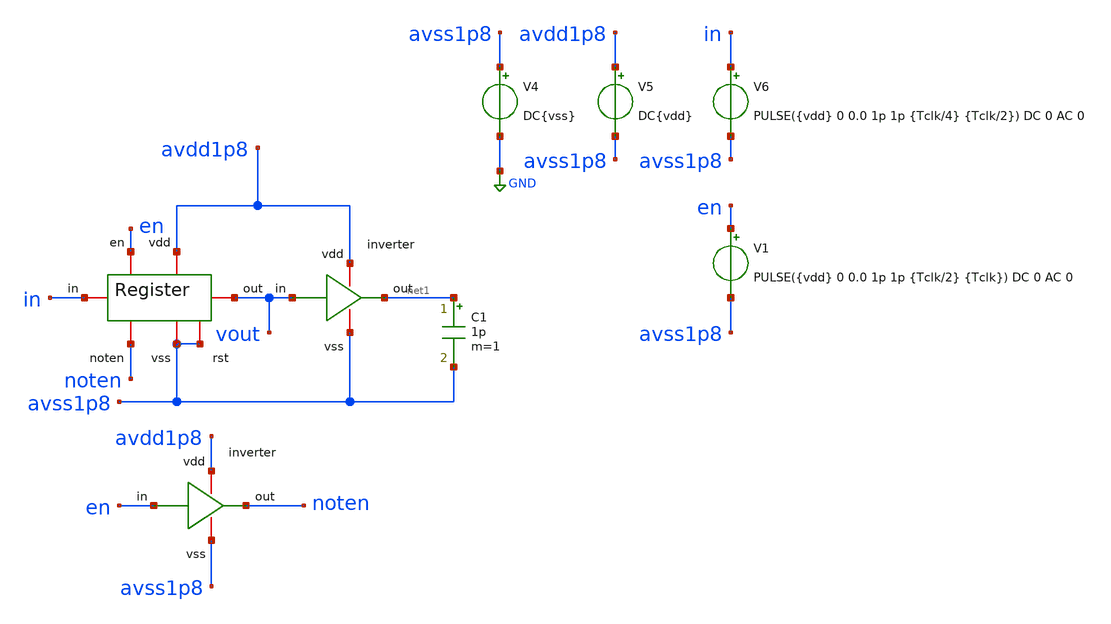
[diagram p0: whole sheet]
** sch_path: verification/testbenches/tb_register.sch
**.subckt tb_register
C1 net1 avss1p8 1p m=1
V4 avss1p8 GND DC{vss}
V5 avdd1p8 avss1p8 DC{vdd}
V6 in avss1p8 PULSE({vdd} 0 0.0 1p 1p {Tclk/4} {Tclk/2}) DC 0 AC 0
x2 avdd1p8 net1 vout avss1p8 inverter
V1 en avss1p8 PULSE({vdd} 0 0.0 1p 1p {Tclk/2} {Tclk}) DC 0 AC 0
x3 avdd1p8 noten en avss1p8 inverter
x1 en noten avss1p8 avdd1p8 vout in avss1p8 register
**** begin user architecture code


* Circuit Parameters
.param vdd = 1.2
.param vss = 0.0
.param Tclk = 10n
.options TEMP = 27.0
* Include Models - IHP SG13G2
.lib cornerMOSlv.lib mos_tt
* OP Parameters & Singals to save
.save all
*Simulations
.control
tran 0.01u 100n
setplot tran1
plot v(en) v(in) + 1.2 v(vout) + 2.4
set filetype = ascii
write dcsweep.raw
.endc
.end


**** end user architecture code
**.ends

* expanding   symbol:  blocks/inverter/schematic/inverter.sym # of pins=4
** sym_path: design/blocks/inverter/schematic/inverter.sym
** sch_path: design/blocks/inverter/schematic/inverter.sch
.subckt inverter vdd out in vss
*.iopin vdd
*.iopin out
*.iopin vss
*.iopin in
XM1 out in vss vss sky130_fd_pr__nfet_01v8 L=0.15 W=0.75 nf=1 ad='int((nf+1)/2) * W/nf * 0.29' as='int((nf+2)/2) * W/nf * 0.29'
+ pd='2*int((nf+1)/2) * (W/nf + 0.29)' ps='2*int((nf+2)/2) * (W/nf + 0.29)' nrd='0.29 / W' nrs='0.29 / W'
+ sa=0 sb=0 sd=0 mult=1 m=1
XM2 out in vdd vdd sky130_fd_pr__pfet_01v8 L=0.15 W=1.5 nf=1 ad='int((nf+1)/2) * W/nf * 0.29' as='int((nf+2)/2) * W/nf * 0.29'
+ pd='2*int((nf+1)/2) * (W/nf + 0.29)' ps='2*int((nf+2)/2) * (W/nf + 0.29)' nrd='0.29 / W' nrs='0.29 / W'
+ sa=0 sb=0 sd=0 mult=1 m=1
.ends


* expanding   symbol:  blocks/register/schematic/register.sym # of pins=7
** sym_path: design/blocks/register/schematic/register.sym
** sch_path: design/blocks/register/schematic/register.sch
.subckt register en noten vss vdd out in rst
*.iopin in
*.iopin vdd
*.iopin vss
*.iopin en
*.iopin noten
*.iopin out
*.iopin rst
x1 vdd net1 in vss inverter
x3 vdd net3 net2 vss inverter
x4 vdd net4 net3 vss inverter
x5 net1 vdd noten net2 vss en transmissiongate
x6 net4 vdd en net2 vss noten transmissiongate
x2 vss vdd nrst net3 vss rst transmissiongate
x8 vss nrst rst vss inverter
x7 vdd net5 net3 vss inverter
x9 vdd out net6 vss inverter
x10 vdd net7 out vss inverter
x11 net5 vdd en net6 vss noten transmissiongate
x12 net7 vdd noten net6 vss en transmissiongate
x13 vss vdd nrst out vss rst transmissiongate
.ends


* expanding   symbol:  blocks/transmissiongate/schematic/transmissiongate.sym # of pins=6
** sym_path: design/blocks/transmissiongate/schematic/transmissiongate.sym
** sch_path: design/blocks/transmissiongate/schematic/transmissiongate.sch
.subckt transmissiongate in vdd noten out vss en
*.iopin noten
*.iopin en
*.iopin in
*.iopin out
*.iopin vdd
*.iopin vss
XM1 out noten in vdd sg13_lv_pmos w=1.5u l=0.15u ng=1 m=1 mm_ok=1
XM2 out en in vss sg13_lv_nmos w=0.75u l=0.15u ng=1 m=1 mm_ok=1
.ends

.GLOBAL GND
.end
